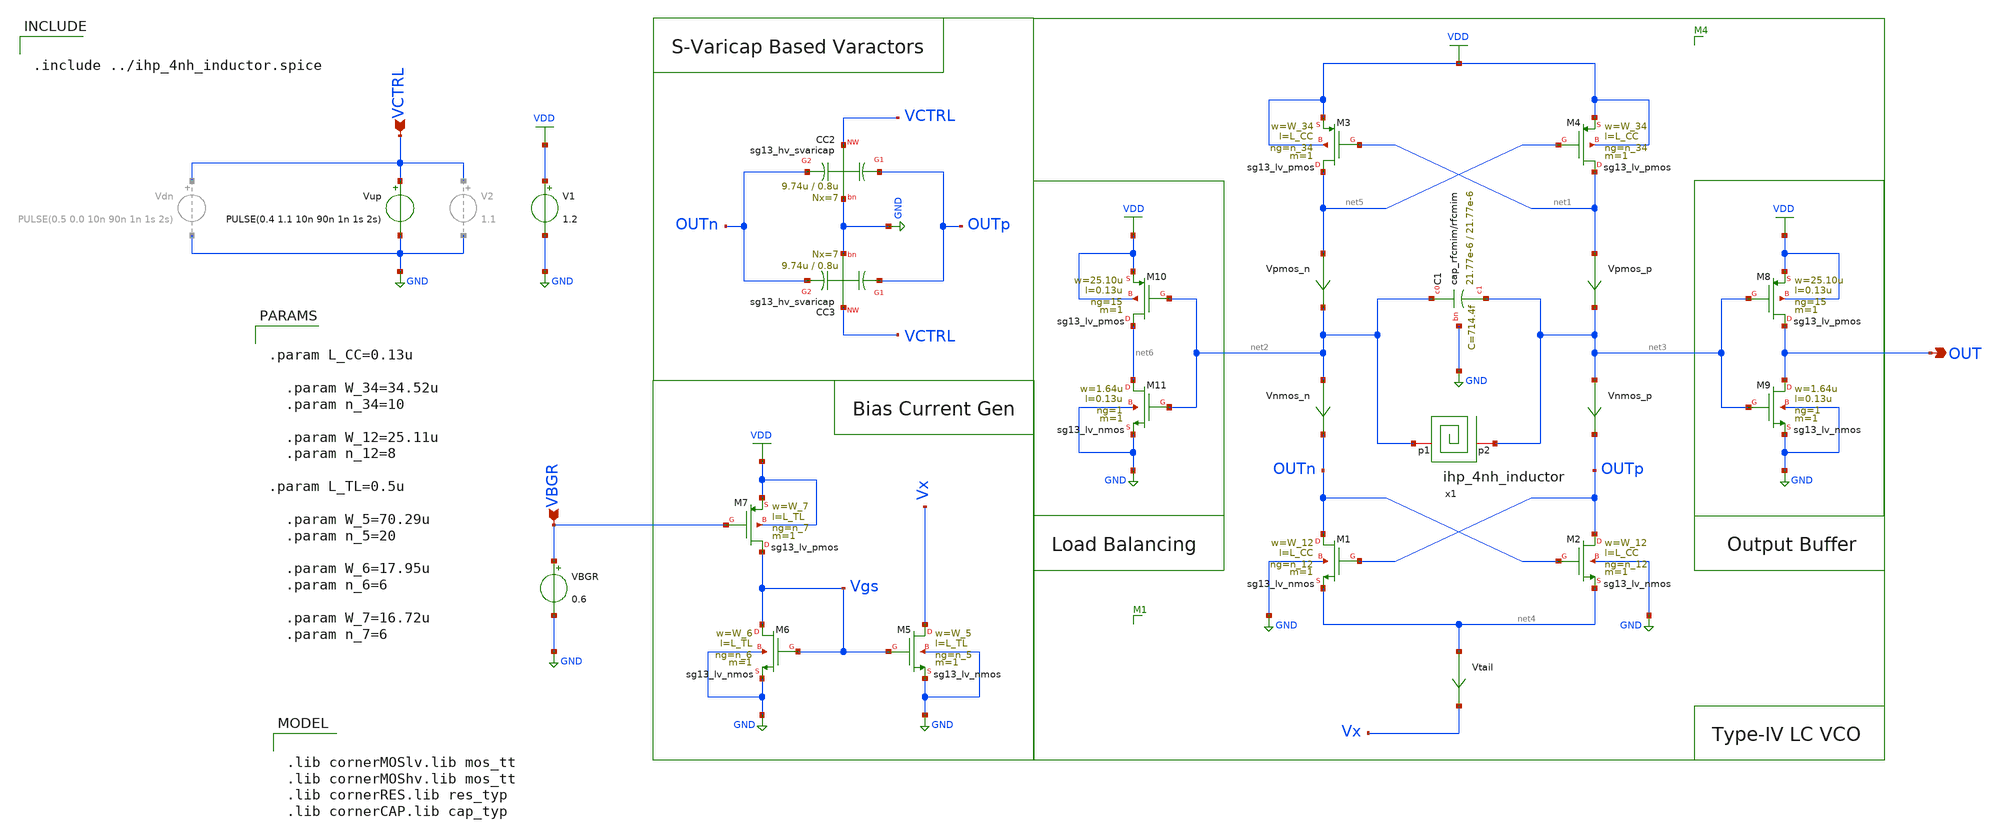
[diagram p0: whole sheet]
** sch_path: schematic/lc-vco/LC_VCO_standalone_tb.sch
**.subckt LC_VCO_standalone_tb OUT VCTRL VBGR
*.opin OUT
*.ipin VCTRL
*.ipin VBGR
XM5 Vx Vgs GND GND sg13_lv_nmos w=W_5 l=L_TL ng=n_5 m=1 mm_ok=1
XM4 net1 net5 VDD VDD sg13_lv_pmos w=W_34 l=L_CC ng=n_34 m=1 mm_ok=1
XM3 net5 net1 VDD VDD sg13_lv_pmos w=W_34 l=L_CC ng=n_34 m=1 mm_ok=1
XM2 OUTp OUTn net4 GND sg13_lv_nmos w=W_12 l=L_CC ng=n_12 m=1 mm_ok=1
XM1 OUTn OUTp net4 GND sg13_lv_nmos w=W_12 l=L_CC ng=n_12 m=1 mm_ok=1
V1 VDD GND 1.2
Vpmos_p net1 net3 0
.save i(vpmos_p)
Vnmos_p net3 OUTp 0
.save i(vnmos_p)
Vtail net4 Vx 0
.save i(vtail)
XM6 Vgs Vgs GND GND sg13_lv_nmos w=W_6 l=L_TL ng=n_6 m=1 mm_ok=1
Vpmos_n net5 net2 0
.save i(vpmos_n)
Vnmos_n net2 OUTn 0
.save i(vnmos_n)
x1 net2 net3 ihp_4nh_inductor
Vup VCTRL GND PULSE(0.4 1.1 10n 90n 1n 1s 2s)
XC1 net2 net3 GND cap_rfcmim w=21.77e-6 l=21.77e-6 wfeed=10.0e-6 m=1 mm_ok=1
XC3 OUTp VCTRL OUTn GND sg13_hv_svaricap w=9.74u l=0.8u Nx=7
XC2 OUTp VCTRL OUTn GND sg13_hv_svaricap w=9.74u l=0.8u Nx=7
XM7 Vgs VBGR VDD VDD sg13_lv_pmos w=W_7 l=L_TL ng=n_7 m=1 mm_ok=1
VBGR VBGR GND 0.6
XM8 OUT net3 VDD VDD sg13_lv_pmos w=25.10u l=0.13u ng=15 m=1 mm_ok=1
XM9 OUT net3 GND GND sg13_lv_nmos w=1.64u l=0.13u ng=1 m=1 mm_ok=1
XM10 net6 net2 VDD VDD sg13_lv_pmos w=25.10u l=0.13u ng=15 m=1 mm_ok=1
XM11 net6 net2 GND GND sg13_lv_nmos w=1.64u l=0.13u ng=1 m=1 mm_ok=1
**** begin user architecture code

.lib cornerMOSlv.lib mos_tt
.lib cornerMOShv.lib mos_tt
.lib cornerRES.lib res_typ
.lib cornerCAP.lib cap_typ



.param L_CC=0.13u

  .param W_34=34.52u
  .param n_34=10

  .param W_12=25.11u
  .param n_12=8

.param L_TL=0.5u

  .param W_5=70.29u
  .param n_5=20

  .param W_6=17.95u
  .param n_6=6

  .param W_7=16.72u
  .param n_7=6



.include ../ihp_4nh_inductor.spice




.param temp = 27
.options method=gear, rshunt=1.0e12

.control

* Save required signals
save v(OUTp) v(VCTRL) v(OUT) v(Vx)

* Long transient simulation
tran 10p 500n 100n

* Save raw waveform
write LC_VCO_standalone_tran.raw

* Plot transient waveform
let vout = v(OUT)
plot v(OUTp) v(VCTRL) v(Vx) v(OUT)

* Plot steady-state waveform
plot v(OUTp) v(VCTRL) v(Vx) v(OUT) xlimit 400n 405n

* FFT analysis
setplot tran1
linearize vout
set specwindow=blackman
fft vout

* Plot FFT spectrum
let power_out_db = db(vout)
plot power_out_db xlimit 2.38G 2.58G ylimit -200 0

* Find the maximum magnitude value between 2G and 3G
meas sp max_power_out_db max power_out_db FROM=2G TO=3G

* Save FFT data
wrdata fft_output_standalone.txt frequency power_out_db

* Save waveform for external processing
wrdata vco_waveform_standalone.txt power_out_db

.endc






.include LC_VCO_standalone_tb.save
.param temp=27
.control
save all
op
write LC_VCO_standalone_tb.raw
.endc



**** end user architecture code
**.ends
.GLOBAL VDD
.GLOBAL GND
.end
